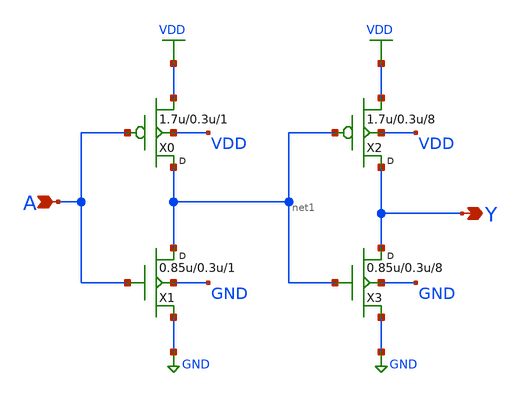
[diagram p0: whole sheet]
** sch_path: lib/12T/clkbuf8/gf180mcu_osu_sc_clkbuf_8.sch
**.subckt gf180mcu_osu_sc_clkbuf_8 A Y
*.ipin A
*.opin Y
X0 net1 A VDD VDD pmos_3p3 w=1.7u l=0.3u m=1
X1 net1 A GND GND nmos_3p3 w=0.85u l=0.3u m=1
X2 Y net1 VDD VDD pmos_3p3 w=1.7u l=0.3u m=8
X3 Y net1 GND GND nmos_3p3 w=0.85u l=0.3u m=8
**.ends
.GLOBAL VDD
.GLOBAL GND
.end
